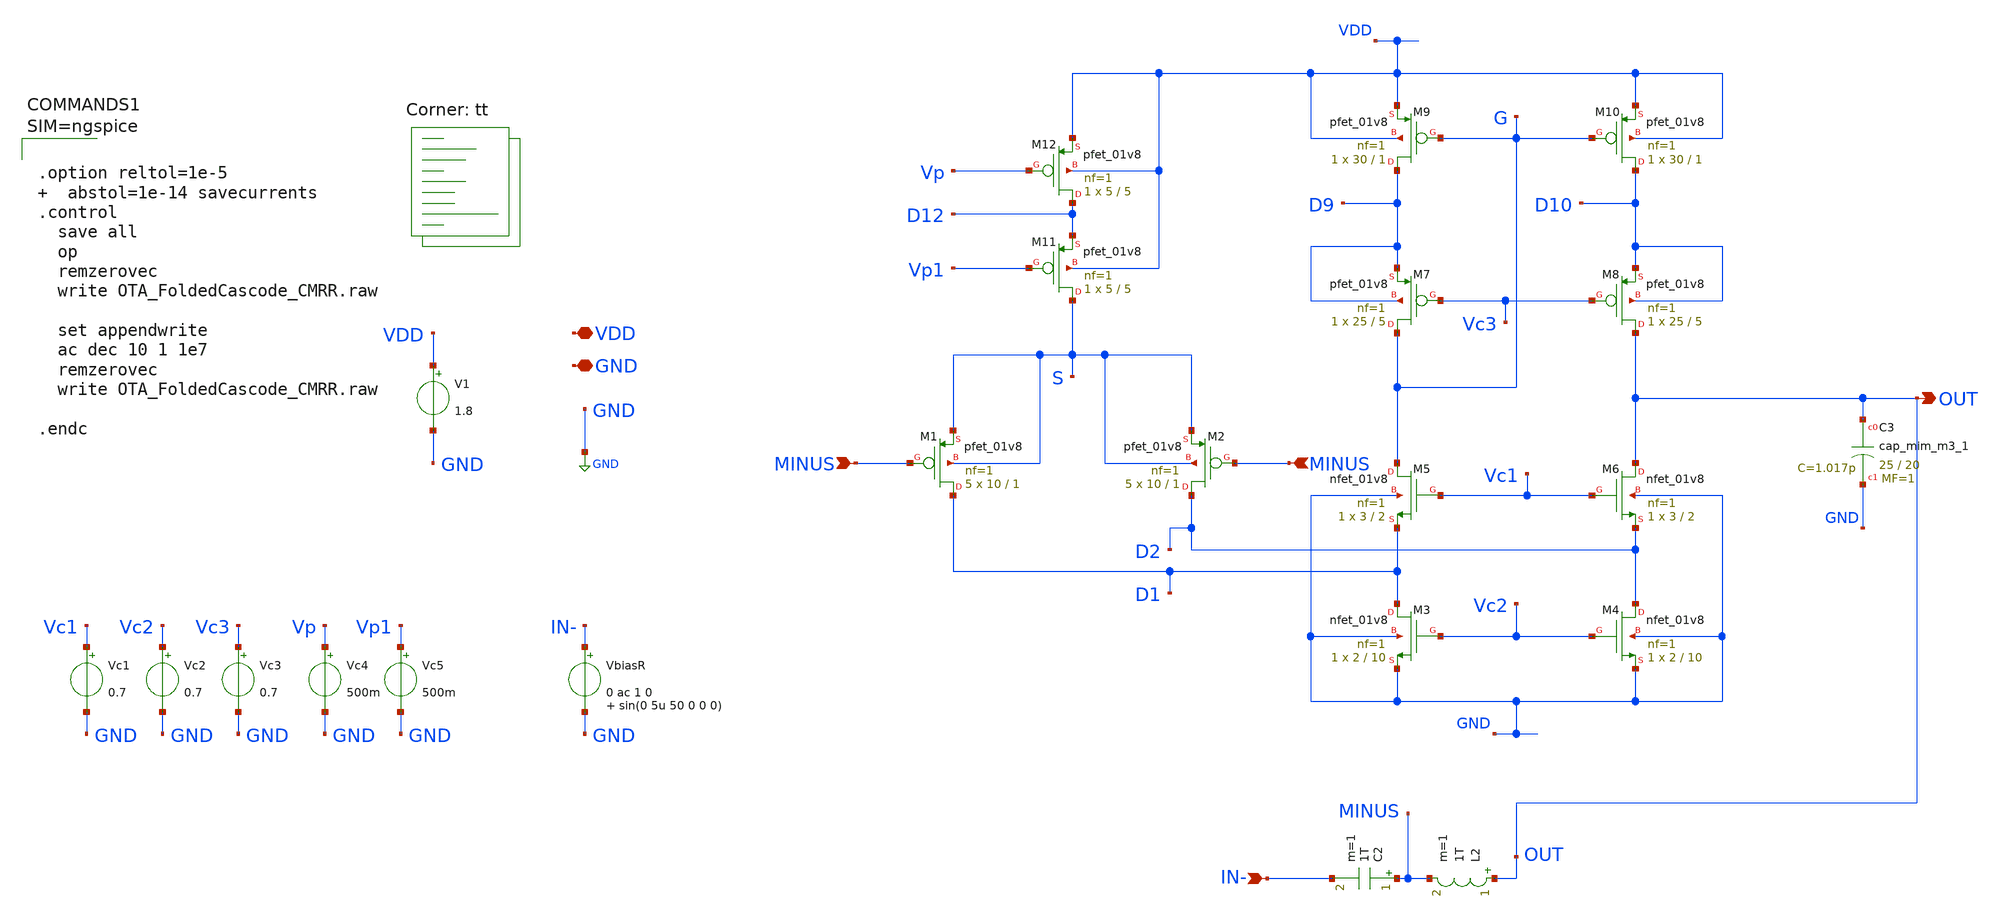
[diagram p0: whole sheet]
** sch_path: xschem/OTA_FoldedCascode_CMRR.sch
**.subckt OTA_FoldedCascode_CMRR VDD GND IN- MINUS MINUS OUT
*.iopin VDD
*.iopin GND
*.ipin IN-
*.ipin MINUS
*.ipin MINUS
*.opin OUT
V1 VDD GND 1.8
VbiasR IN- GND 0 ac 1 0 sin(0 5u 50 0 0 0)
Vc1 Vc1 GND 0.7
Vc2 Vc2 GND 0.7
Vc3 Vc3 GND 0.7
C2 MINUS IN- 1T m=1
L2 OUT MINUS 1T m=1
XM1 D1 MINUS S S sky130_fd_pr__pfet_01v8 L=1 W=10 nf=1 ad='int((nf+1)/2) * W/nf * 0.29' as='int((nf+2)/2) * W/nf * 0.29'
+ pd='2*int((nf+1)/2) * (W/nf + 0.29)' ps='2*int((nf+2)/2) * (W/nf + 0.29)' nrd='0.29 / W' nrs='0.29 / W'
+ sa=0 sb=0 sd=0 mult=5 m=5
XM2 D2 MINUS S S sky130_fd_pr__pfet_01v8 L=1 W=10 nf=1 ad='int((nf+1)/2) * W/nf * 0.29' as='int((nf+2)/2) * W/nf * 0.29'
+ pd='2*int((nf+1)/2) * (W/nf + 0.29)' ps='2*int((nf+2)/2) * (W/nf + 0.29)' nrd='0.29 / W' nrs='0.29 / W'
+ sa=0 sb=0 sd=0 mult=5 m=5
XM3 D1 Vc2 GND GND sky130_fd_pr__nfet_01v8 L=10 W=2 nf=1 ad='int((nf+1)/2) * W/nf * 0.29' as='int((nf+2)/2) * W/nf * 0.29'
+ pd='2*int((nf+1)/2) * (W/nf + 0.29)' ps='2*int((nf+2)/2) * (W/nf + 0.29)' nrd='0.29 / W' nrs='0.29 / W'
+ sa=0 sb=0 sd=0 mult=1 m=1
XM4 D2 Vc2 GND GND sky130_fd_pr__nfet_01v8 L=10 W=2 nf=1 ad='int((nf+1)/2) * W/nf * 0.29' as='int((nf+2)/2) * W/nf * 0.29'
+ pd='2*int((nf+1)/2) * (W/nf + 0.29)' ps='2*int((nf+2)/2) * (W/nf + 0.29)' nrd='0.29 / W' nrs='0.29 / W'
+ sa=0 sb=0 sd=0 mult=1 m=1
XM5 G Vc1 D1 GND sky130_fd_pr__nfet_01v8 L=2 W=3 nf=1 ad='int((nf+1)/2) * W/nf * 0.29' as='int((nf+2)/2) * W/nf * 0.29'
+ pd='2*int((nf+1)/2) * (W/nf + 0.29)' ps='2*int((nf+2)/2) * (W/nf + 0.29)' nrd='0.29 / W' nrs='0.29 / W'
+ sa=0 sb=0 sd=0 mult=1 m=1
XM6 OUT Vc1 D2 GND sky130_fd_pr__nfet_01v8 L=2 W=3 nf=1 ad='int((nf+1)/2) * W/nf * 0.29' as='int((nf+2)/2) * W/nf * 0.29'
+ pd='2*int((nf+1)/2) * (W/nf + 0.29)' ps='2*int((nf+2)/2) * (W/nf + 0.29)' nrd='0.29 / W' nrs='0.29 / W'
+ sa=0 sb=0 sd=0 mult=1 m=1
XM7 G Vc3 D9 D9 sky130_fd_pr__pfet_01v8 L=5 W=25 nf=1 ad='int((nf+1)/2) * W/nf * 0.29' as='int((nf+2)/2) * W/nf * 0.29'
+ pd='2*int((nf+1)/2) * (W/nf + 0.29)' ps='2*int((nf+2)/2) * (W/nf + 0.29)' nrd='0.29 / W' nrs='0.29 / W'
+ sa=0 sb=0 sd=0 mult=1 m=1
XM8 OUT Vc3 D10 D10 sky130_fd_pr__pfet_01v8 L=5 W=25 nf=1 ad='int((nf+1)/2) * W/nf * 0.29' as='int((nf+2)/2) * W/nf * 0.29'
+ pd='2*int((nf+1)/2) * (W/nf + 0.29)' ps='2*int((nf+2)/2) * (W/nf + 0.29)' nrd='0.29 / W' nrs='0.29 / W'
+ sa=0 sb=0 sd=0 mult=1 m=1
XM9 D9 G VDD VDD sky130_fd_pr__pfet_01v8 L=1 W=30 nf=1 ad='int((nf+1)/2) * W/nf * 0.29' as='int((nf+2)/2) * W/nf * 0.29'
+ pd='2*int((nf+1)/2) * (W/nf + 0.29)' ps='2*int((nf+2)/2) * (W/nf + 0.29)' nrd='0.29 / W' nrs='0.29 / W'
+ sa=0 sb=0 sd=0 mult=1 m=1
XM10 D10 G VDD VDD sky130_fd_pr__pfet_01v8 L=1 W=30 nf=1 ad='int((nf+1)/2) * W/nf * 0.29' as='int((nf+2)/2) * W/nf * 0.29'
+ pd='2*int((nf+1)/2) * (W/nf + 0.29)' ps='2*int((nf+2)/2) * (W/nf + 0.29)' nrd='0.29 / W' nrs='0.29 / W'
+ sa=0 sb=0 sd=0 mult=1 m=1
XM11 S Vp1 D12 VDD sky130_fd_pr__pfet_01v8 L=5 W=5 nf=1 ad='int((nf+1)/2) * W/nf * 0.29' as='int((nf+2)/2) * W/nf * 0.29'
+ pd='2*int((nf+1)/2) * (W/nf + 0.29)' ps='2*int((nf+2)/2) * (W/nf + 0.29)' nrd='0.29 / W' nrs='0.29 / W'
+ sa=0 sb=0 sd=0 mult=1 m=1
XM12 D12 Vp VDD VDD sky130_fd_pr__pfet_01v8 L=5 W=5 nf=1 ad='int((nf+1)/2) * W/nf * 0.29' as='int((nf+2)/2) * W/nf * 0.29'
+ pd='2*int((nf+1)/2) * (W/nf + 0.29)' ps='2*int((nf+2)/2) * (W/nf + 0.29)' nrd='0.29 / W' nrs='0.29 / W'
+ sa=0 sb=0 sd=0 mult=1 m=1
XC3 OUT GND sky130_fd_pr__cap_mim_m3_1 W=25 L=20 MF=1 m=1
Vc4 Vp GND 500m
Vc5 Vp1 GND 500m
**** begin user architecture code



.option reltol=1e-5   abstol=1e-14 savecurrents
.control
  save all
  op
  remzerovec
  write OTA_FoldedCascode_CMRR.raw

  set appendwrite
  ac dec 10 1 1e7
  remzerovec
  write OTA_FoldedCascode_CMRR.raw

.endc



.lib $::SKYWATER_MODELS/sky130.lib.spice tt
**** end user architecture code
**.ends
.GLOBAL GND
.end
